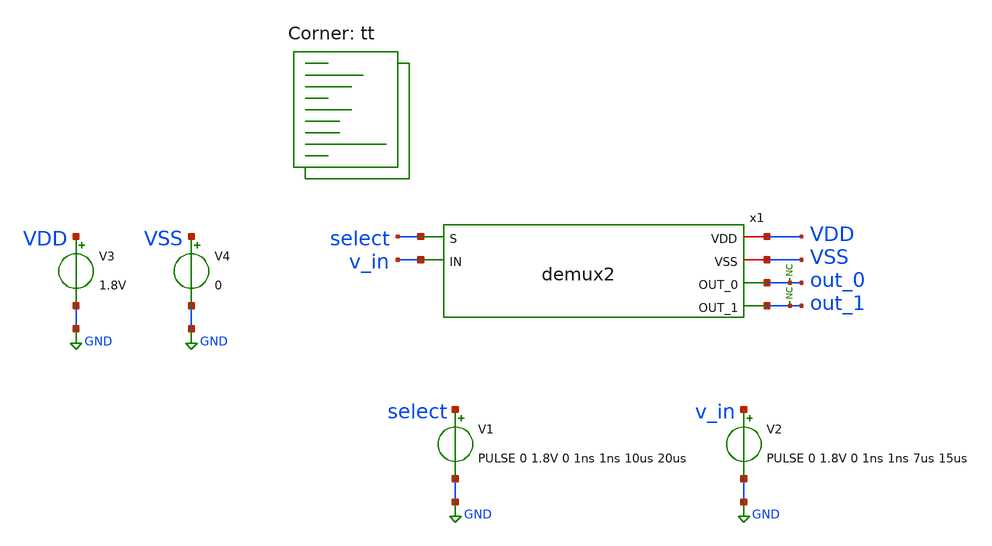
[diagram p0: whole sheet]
** sch_path: xschem/tests/demux2/demux2_test.sch
**.subckt demux2_test
V3 VDD GND 1.8V
V4 VSS GND 0
x1 select VDD VSS out_0 v_in out_1 demux2
V1 select GND PULSE 0 1.8V 0 1ns 1ns 10us 20us
V2 v_in GND PULSE 0 1.8V 0 1ns 1ns 7us 15us
* noconn out_0
* noconn out_1
**** begin user architecture code

*.lib $::SKYWATER_MODELS/sky130.lib.spice tt
.include $::SKYWATER_STDCELLS/sky130_fd_sc_hd.spice




* ngspice commands
.options acct list
.temp 25
*vvcc VDD 0 dc 1.8
*vvss VSS 0 0
.control
save all
tran 0.1u 100u
plot select v_in+2 out_0+4 out_1+6
write pulse_generator_test.raw
.endc






.lib $::SKYWATER_MODELS/sky130.lib.spice tt
**** end user architecture code
**.ends

* expanding   symbol:  src/demux2/demux2.sym # of pins=6
** sym_path: xschem/src/demux2/demux2.sym
** sch_path: xschem/src/demux2/demux2.sch
.subckt demux2 S VDD VSS OUT_0 IN OUT_1
*.ipin S
*.opin OUT_0
*.ipin IN
*.opin OUT_1
*.iopin VDD
*.iopin VSS
x1 net1 IN VSS VSS VDD VDD OUT_0 sky130_fd_sc_hd__and2_0
x2 S IN VSS VSS VDD VDD OUT_1 sky130_fd_sc_hd__and2_0
x3 S VSS VSS VDD VDD net1 sky130_fd_sc_hd__inv_1
.ends

.GLOBAL GND
.end
